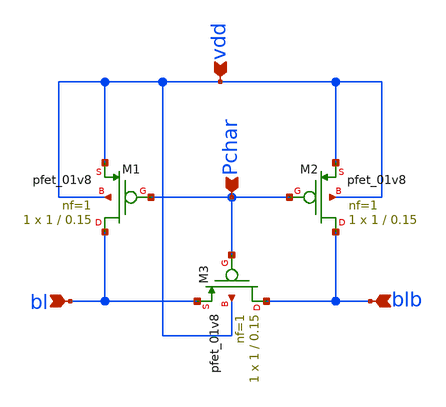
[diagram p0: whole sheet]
** sch_path: Projects/Schematic_Design_and_Analysis_of_an_8-Word_8-Bit_Static_RAM_with_6T_Storage_Cells_using_SKY130PDK/assets/schematic/precharge.sch
**.subckt precharge vdd Pchar blb bl
*.ipin vdd
*.ipin Pchar
*.ipin blb
*.ipin bl
XM1 bl Pchar vdd vdd sky130_fd_pr__pfet_01v8 L=0.15 W=1 nf=1 ad='int((nf+1)/2) * W/nf * 0.29' as='int((nf+2)/2) * W/nf * 0.29'
+ pd='2*int((nf+1)/2) * (W/nf + 0.29)' ps='2*int((nf+2)/2) * (W/nf + 0.29)' nrd='0.29 / W' nrs='0.29 / W'
+ sa=0 sb=0 sd=0 mult=1 m=1
XM2 blb Pchar vdd vdd sky130_fd_pr__pfet_01v8 L=0.15 W=1 nf=1 ad='int((nf+1)/2) * W/nf * 0.29' as='int((nf+2)/2) * W/nf * 0.29'
+ pd='2*int((nf+1)/2) * (W/nf + 0.29)' ps='2*int((nf+2)/2) * (W/nf + 0.29)' nrd='0.29 / W' nrs='0.29 / W'
+ sa=0 sb=0 sd=0 mult=1 m=1
XM3 blb Pchar bl vdd sky130_fd_pr__pfet_01v8 L=0.15 W=1 nf=1 ad='int((nf+1)/2) * W/nf * 0.29' as='int((nf+2)/2) * W/nf * 0.29'
+ pd='2*int((nf+1)/2) * (W/nf + 0.29)' ps='2*int((nf+2)/2) * (W/nf + 0.29)' nrd='0.29 / W' nrs='0.29 / W'
+ sa=0 sb=0 sd=0 mult=1 m=1
**.ends
.end
